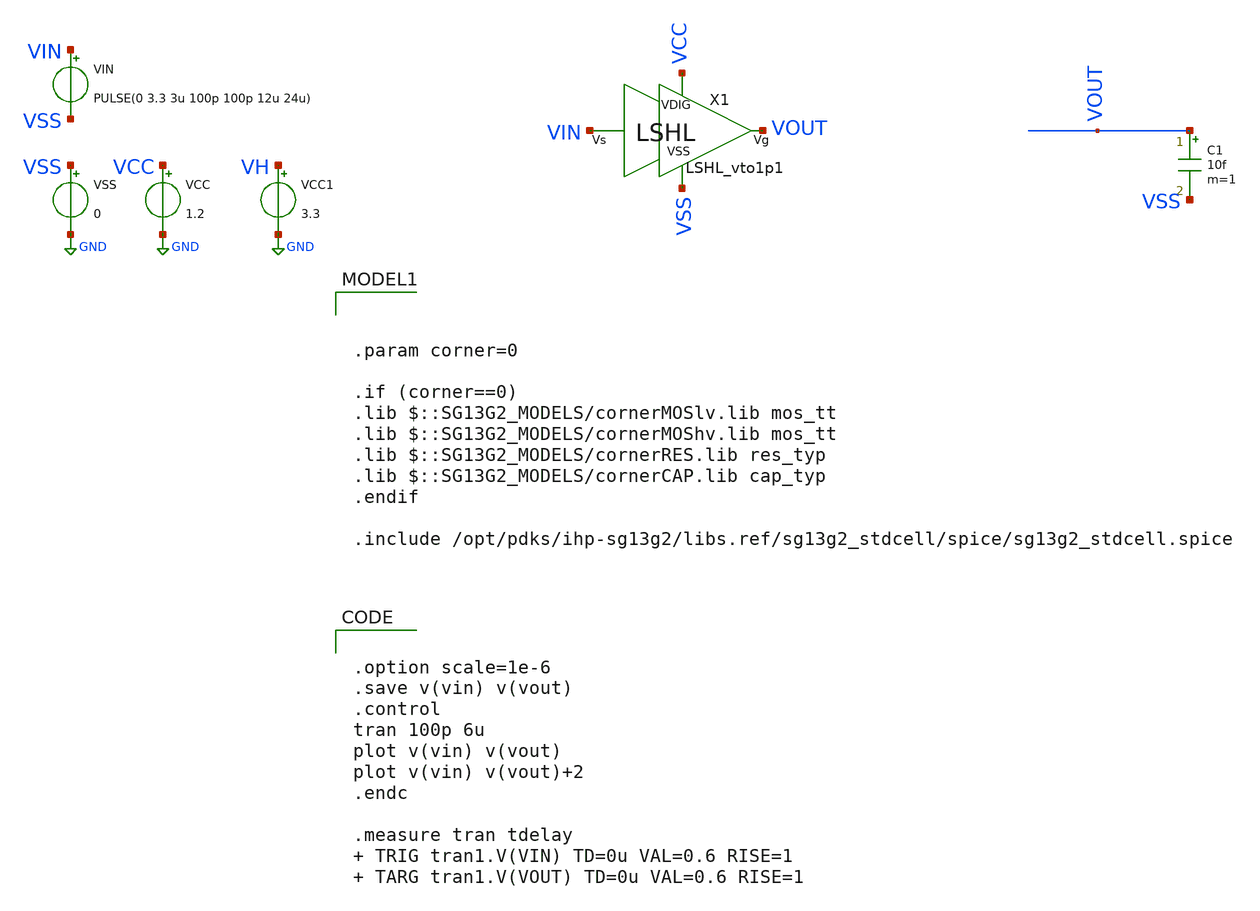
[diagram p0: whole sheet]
** sch_path: AC3E_USM_TDBUCK/design_data/xschem/LSHL/tb_LSHL_vto1p1.sch
* IHP-GmbH/IHP-Open-PDK/ihp-sg13g2/libs.tech/xschem/sg13g2_stdcells/sg13g2_buf_4.sch:
* Copyright 2023 IHP PDK Authors
* Licensed under the Apache License, Version 2.0 (the "License");
**.subckt tb_LSHL_vto1p1
VCC VCC GND 1.2
VSS VSS GND 0
VIN VIN VSS PULSE(0 3.3 3u 100p 100p 12u 24u)
C1 VOUT VSS 10f m=1
X1 VIN VOUT VCC VSS LSHL_vto1p1
VCC1 VH GND 3.3
**** begin user architecture code


.option scale=1e-6
.save v(vin) v(vout)
.control
tran 100p 6u
plot v(vin) v(vout)
plot v(vin) v(vout)+2
.endc

.measure tran tdelay  TRIG tran1.V(VIN) TD=0u VAL=0.6 RISE=1  TARG tran1.V(VOUT) TD=0u VAL=0.6
+ RISE=1






.param corner=0

.if (corner==0)
.lib $::SG13G2_MODELS/cornerMOSlv.lib mos_tt
.lib $::SG13G2_MODELS/cornerMOShv.lib mos_tt
.lib $::SG13G2_MODELS/cornerRES.lib res_typ
.lib $::SG13G2_MODELS/cornerCAP.lib cap_typ
.endif

.include /opt/pdks/ihp-sg13g2/libs.ref/sg13g2_stdcell/spice/sg13g2_stdcell.spice

**** end user architecture code
**.ends

* expanding   symbol:  LSHL_vto1p1.sym # of pins=4
** sym_path: AC3E_USM_TDBUCK/design_data/xschem/LSHL/LSHL_vto1p1.sym
** sch_path: AC3E_USM_TDBUCK/design_data/xschem/LSHL/LSHL_vto1p1.sch
.subckt LSHL_vto1p1 Vs Vg VDIG VSS
*.iopin VDIG
*.ipin Vs
*.opin Vg
*.iopin VSS
XMD5 VgMD2 Vs VDIG VDIG sg13_hv_pmos w=1u l=0.4u ng=1 m=2 mm_ok=1
XMD6 VSS Vs VgMD2 VSS sg13_hv_nmos w=1u l=0.45u ng=1 m=1 mm_ok=1
x7 Vg net1 VDIG VSS sg13g2_buf_4
x1 net1 VgMD2 VDIG VSS sg13g2_inv_1
.ends


* expanding   symbol:  sg13g2_stdcells/sg13g2_buf_4.sym # of pins=2
** sym_path: sg13g2_stdcells/sg13g2_buf_4.sym
** sch_path: sg13g2_stdcells/sg13g2_buf_4.sch
.subckt sg13g2_buf_4 X A VDD VSS
*.ipin A
*.opin X
*.iopin VDD
*.iopin VSS
XM1 net1 A VSS VSS sg13_lv_nmos w=740.00n l=130.00n ng=1 m=1 mm_ok=1
XM2 X net1 VSS VSS sg13_lv_nmos w=2.96u l=130.00n ng=4 m=1 mm_ok=1
XM3 net1 A VDD VDD sg13_lv_pmos w=1.68u l=130.00n ng=2 m=1 mm_ok=1
XM4 X net1 VDD VDD sg13_lv_pmos w=4.48u l=130.00n ng=4 m=1 mm_ok=1
.ends


* expanding   symbol:  sg13g2_stdcells/sg13g2_inv_1.sym # of pins=2
** sym_path: sg13g2_stdcells/sg13g2_inv_1.sym
** sch_path: sg13g2_stdcells/sg13g2_inv_1.sch
.subckt sg13g2_inv_1 Y A VDD VSS
*.opin Y
*.ipin A
*.iopin VDD
*.iopin VSS
XM1 Y A VSS VSS sg13_lv_nmos w=740.00n l=130.00n ng=1 m=1 mm_ok=1
XM2 Y A VDD VDD sg13_lv_pmos w=1.12u l=130.00n ng=1 m=1 mm_ok=1
.ends

.GLOBAL GND
.end
